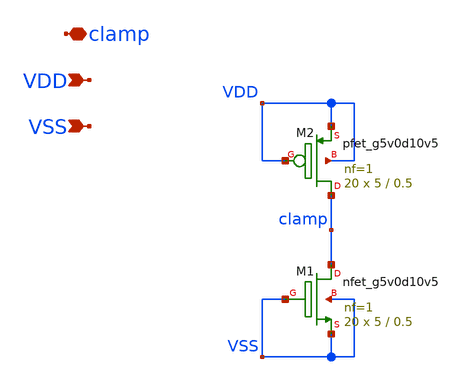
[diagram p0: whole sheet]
** sch_path: designs/esd_cell.sch
**.subckt esd_cell clamp VDD VSS
*.iopin clamp
*.ipin VDD
*.ipin VSS
XM1 clamp VSS VSS VSS sky130_fd_pr__nfet_g5v0d10v5 L=0.5 W=5 nf=1 ad='int((nf+1)/2) * W/nf * 0.29' as='int((nf+2)/2) * W/nf * 0.29'
+ pd='2*int((nf+1)/2) * (W/nf + 0.29)' ps='2*int((nf+2)/2) * (W/nf + 0.29)' nrd='0.29 / W' nrs='0.29 / W'
+ sa=0 sb=0 sd=0 mult=20 m=20
XM2 clamp VDD VDD VDD sky130_fd_pr__pfet_g5v0d10v5 L=0.5 W=5 nf=1 ad='int((nf+1)/2) * W/nf * 0.29' as='int((nf+2)/2) * W/nf * 0.29'
+ pd='2*int((nf+1)/2) * (W/nf + 0.29)' ps='2*int((nf+2)/2) * (W/nf + 0.29)' nrd='0.29 / W' nrs='0.29 / W'
+ sa=0 sb=0 sd=0 mult=20 m=20
**.ends
.end
